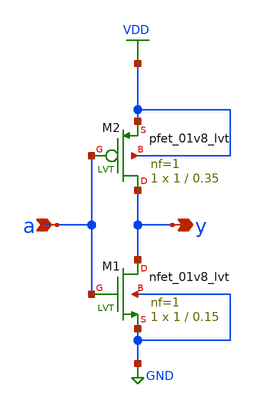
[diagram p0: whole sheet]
** sch_path: xschem/not.sch
* Copyright 2021 Stefan Frederik Schippers
* Licensed under the Apache License, Version 2.0 (the "License");
* you may not use this file except in compliance with the License.
* You may obtain a copy of the License at
* https://www.apache.org/licenses/LICENSE-2.0
* Unless required by applicable law or agreed to in writing, software
* distributed under the License is distributed on an "AS IS" BASIS,
* WITHOUT WARRANTIES OR CONDITIONS OF ANY KIND, either express or implied.
* See the License for the specific language governing permissions and
* limitations under the License.
**.subckt not a y
*.ipin a
*.opin y
XM1 y a GND GND sky130_fd_pr__nfet_01v8_lvt L=0.15 W=1 nf=1 ad='int((nf+1)/2) * W/nf * 0.29' as='int((nf+2)/2) * W/nf * 0.29'
+ pd='2*int((nf+1)/2) * (W/nf + 0.29)' ps='2*int((nf+2)/2) * (W/nf + 0.29)' nrd='0.29 / W' nrs='0.29 / W'
+ sa=0 sb=0 sd=0 mult=1 m=1
XM2 y a VDD VDD sky130_fd_pr__pfet_01v8_lvt L=0.35 W=1 nf=1 ad='int((nf+1)/2) * W/nf * 0.29' as='int((nf+2)/2) * W/nf * 0.29'
+ pd='2*int((nf+1)/2) * (W/nf + 0.29)' ps='2*int((nf+2)/2) * (W/nf + 0.29)' nrd='0.29 / W' nrs='0.29 / W'
+ sa=0 sb=0 sd=0 mult=1 m=1
**.ends
.GLOBAL VDD
.GLOBAL GND
.end
